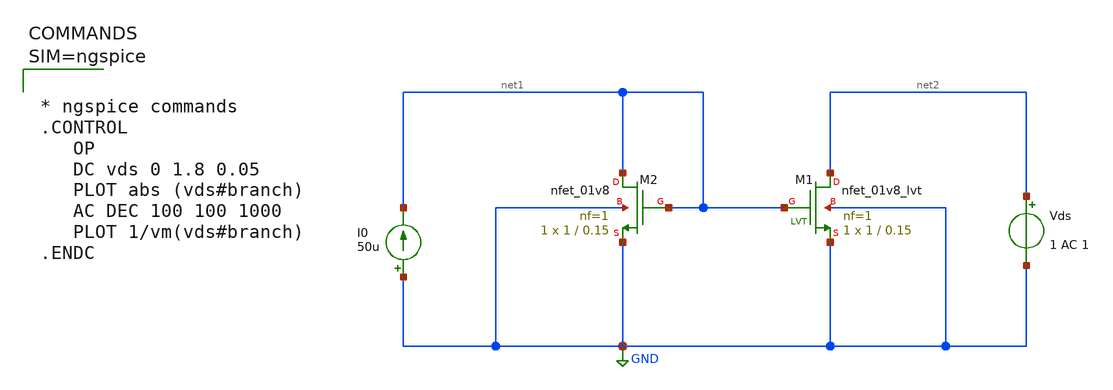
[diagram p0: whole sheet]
** sch_path: xschem/currentmirror.sch
**.subckt currentmirror
I0 GND net1 50u
XM1 net2 net1 GND GND sky130_fd_pr__nfet_01v8_lvt L=0.15 W=1 nf=1 ad='int((1 + 1)/2) * 1 / 1 * 0.29'
+ as='int((1 + 2)/2) * 1 / 1 * 0.29' pd='2*int((1 + 1)/2) * (1 / 1 + 0.29)' ps='2*int((1 + 2)/2) * (1 / 1 + 0.29)'
+ nrd='0.29 / 1 ' nrs='0.29 / 1 ' sa=0 sb=0 sd=0 mult=1 m=1
XM2 net1 net1 GND GND sky130_fd_pr__nfet_01v8 L=0.15 W=1 nf=1 ad='int((1 + 1)/2) * 1 / 1 * 0.29' as='int((1 + 2)/2) * 1 / 1 * 0.29'
+ pd='2*int((1 + 1)/2) * (1 / 1 + 0.29)' ps='2*int((1 + 2)/2) * (1 / 1 + 0.29)' nrd='0.29 / 1 ' nrs='0.29 / 1 '
+ sa=0 sb=0 sd=0 mult=1 m=1
Vds net2 GND 1 AC 1
**** begin user architecture code

** opencircuitdesign pdks install
.lib $::SKYWATER_MODELS/sky130.lib.spice tt




* ngspice commands
.CONTROL
   OP
   DC vds 0 1.8 0.05
   PLOT abs (vds#branch)
   AC DEC 100 100 1000
   PLOT 1/vm(vds#branch)
.ENDC



**** end user architecture code
**.ends
.GLOBAL GND
.end
